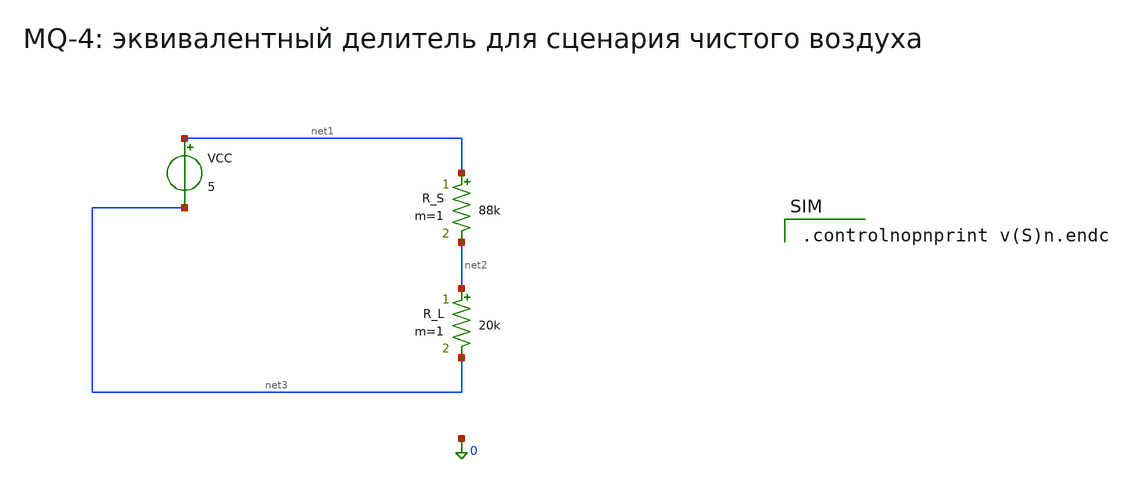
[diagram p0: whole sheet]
** sch_path: docs/figures/xschem_probe/mq4_divider.sch
**.subckt mq4_divider
VCC net1 net3 5
R_S net1 net2 88k m=1
R_L net2 net3 20k m=1
**** begin user architecture code

.controlnopnprint v(S)n.endc

**** end user architecture code
**.ends
.end
